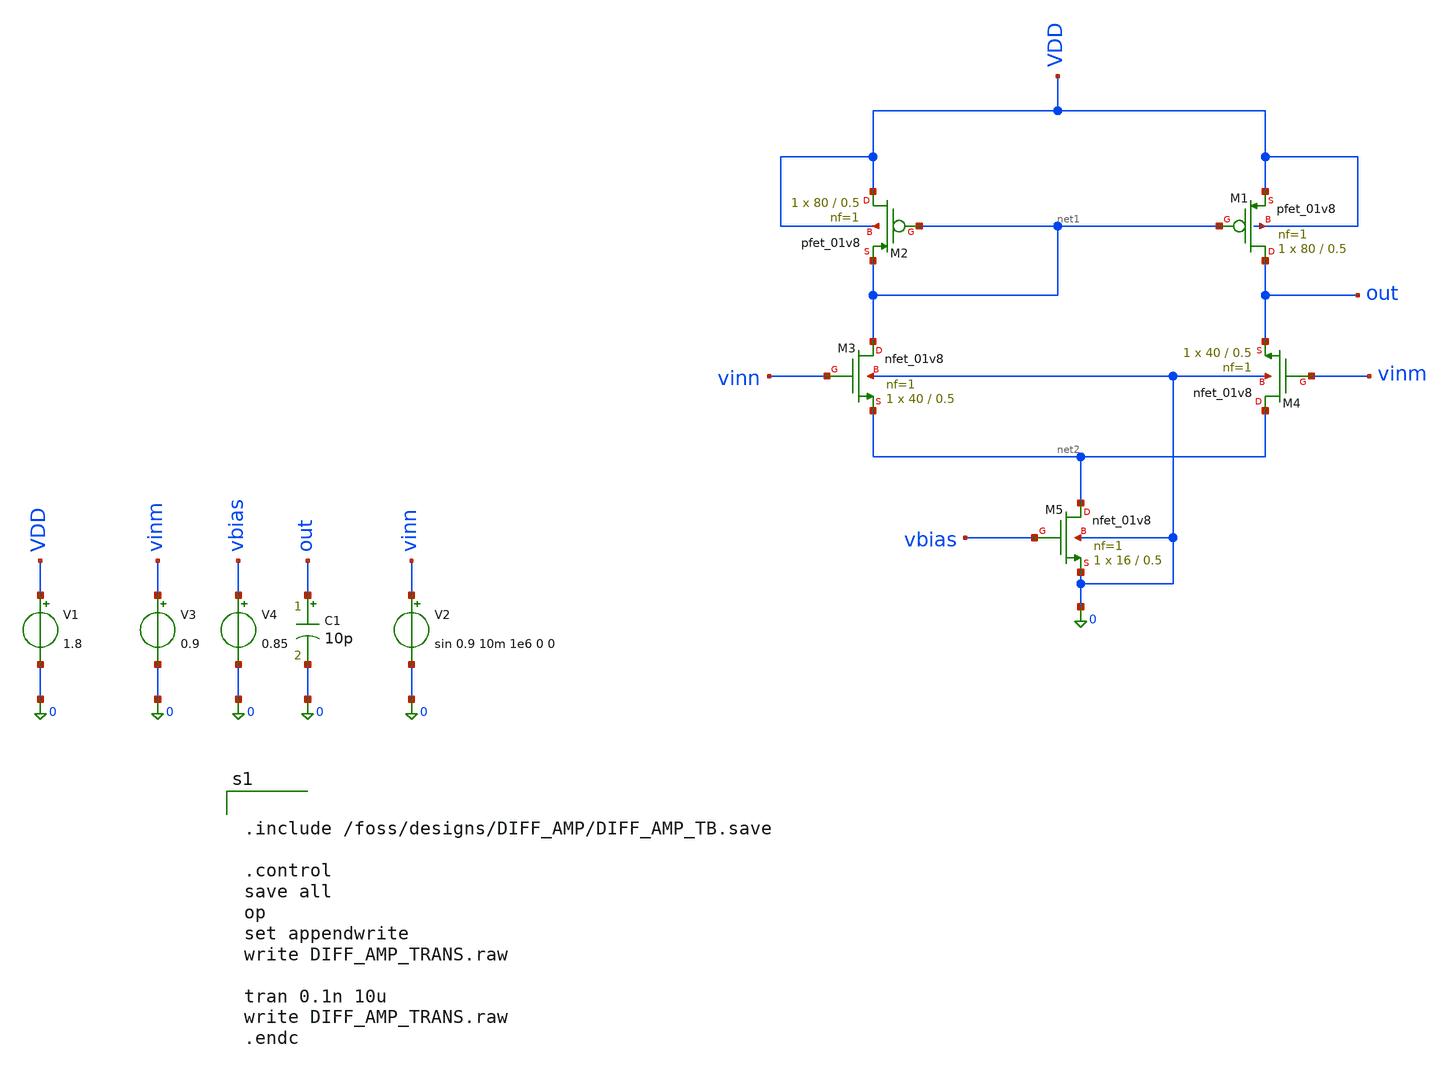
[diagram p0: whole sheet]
** sch_path: new.sch
**.subckt new
V1 VDD 0 1.8
V2 vinn 0 sin 0.9 10m 1e6 0 0
V3 vinm 0 0.9
V4 vbias 0 0.85
C1 out 0 10p m=1
XM1 out net1 VDD VDD sky130_fd_pr__pfet_01v8 L=0.5 W=80 nf=1 ad='int((1 + 1)/2) * 80 / 1 * 0.29' as='int((1 + 2)/2) * 80 / 1 * 0.29'
+ pd='2*int((1 + 1)/2) * (80 / 1 + 0.29)' ps='2*int((1 + 2)/2) * (80 / 1 + 0.29)' nrd='0.29 / 80 ' nrs='0.29 / 80 '
+ sa=0 sb=0 sd=0 mult=1 m=1
XM2 VDD net1 net1 VDD sky130_fd_pr__pfet_01v8 L=0.5 W=80 nf=1 ad='int((1 + 1)/2) * 80 / 1 * 0.29' as='int((1 + 2)/2) * 80 / 1 * 0.29'
+ pd='2*int((1 + 1)/2) * (80 / 1 + 0.29)' ps='2*int((1 + 2)/2) * (80 / 1 + 0.29)' nrd='0.29 / 80 ' nrs='0.29 / 80 '
+ sa=0 sb=0 sd=0 mult=1 m=1
XM3 net1 vinn net2 0 sky130_fd_pr__nfet_01v8 L=0.5 W=40 nf=1 ad='int((1 + 1)/2) * 40 / 1 * 0.29' as='int((1 + 2)/2) * 40 / 1 * 0.29'
+ pd='2*int((1 + 1)/2) * (40 / 1 + 0.29)' ps='2*int((1 + 2)/2) * (40 / 1 + 0.29)' nrd='0.29 / 40 ' nrs='0.29 / 40 '
+ sa=0 sb=0 sd=0 mult=1 m=1
XM4 net2 vinm out 0 sky130_fd_pr__nfet_01v8 L=0.5 W=40 nf=1 ad='int((1 + 1)/2) * 40 / 1 * 0.29' as='int((1 + 2)/2) * 40 / 1 * 0.29'
+ pd='2*int((1 + 1)/2) * (40 / 1 + 0.29)' ps='2*int((1 + 2)/2) * (40 / 1 + 0.29)' nrd='0.29 / 40 ' nrs='0.29 / 40 '
+ sa=0 sb=0 sd=0 mult=1 m=1
XM5 net2 vbias 0 0 sky130_fd_pr__nfet_01v8 L=0.5 W=16 nf=1 ad='int((1 + 1)/2) * 16 / 1 * 0.29' as='int((1 + 2)/2) * 16 / 1 * 0.29'
+ pd='2*int((1 + 1)/2) * (16 / 1 + 0.29)' ps='2*int((1 + 2)/2) * (16 / 1 + 0.29)' nrd='0.29 / 16 ' nrs='0.29 / 16 '
+ sa=0 sb=0 sd=0 mult=1 m=1
**** begin user architecture code

** opencircuitdesign pdks install
.lib $::SKYWATER_MODELS/sky130.lib.spice tt



.include /foss/designs/DIFF_AMP/DIFF_AMP_TB.save

.control
save all
op
set appendwrite
write DIFF_AMP_TRANS.raw

tran 0.1n 10u
write DIFF_AMP_TRANS.raw
.endc


**** end user architecture code
**.ends
.end
